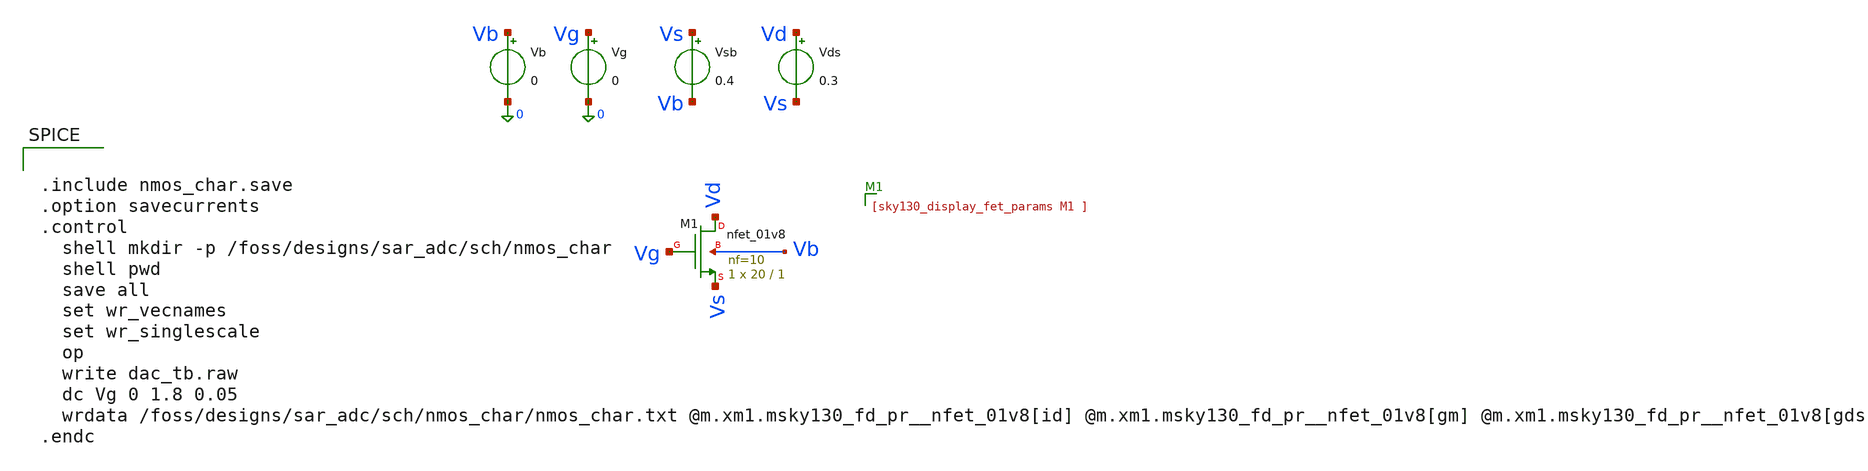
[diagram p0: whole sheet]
** sch_path: sch/archive/old/nmos_char.sch
**.subckt nmos_char
XM1 Vd Vg Vs Vb sky130_fd_pr__nfet_01v8 L=1 W=20 nf=10 ad='int((10 + 1)/2) * 20 / 10 * 0.29' as='int((10 + 2)/2) * 20 / 10 * 0.29'
+ pd='2*int((10 + 1)/2) * (20 / 10 + 0.29)' ps='2*int((10 + 2)/2) * (20 / 10 + 0.29)' nrd='0.29 / 20 '
+ nrs='0.29 / 20 ' sa=0 sb=0 sd=0 mult=1 m=1
Vsb Vs Vb 0.4
.save i(vsb)
Vds Vd Vs 0.3
.save i(vds)
Vb Vb 0 0
.save i(vb)
Vg Vg 0 0
.save i(vg)
**** begin user architecture code

** opencircuitdesign pdks install
.lib $::SKYWATER_MODELS/sky130.lib.spice tt
.include $::SKYWATER_STDCELLS/sky130_fd_sc_hd.spice



.include nmos_char.save
.option savecurrents
.control
  shell mkdir -p /foss/designs/sar_adc/sch/nmos_char
  shell pwd
  save all
  set wr_vecnames
  set wr_singlescale
  op
  write dac_tb.raw
  dc Vg 0 1.8 0.05
  wrdata /foss/designs/sar_adc/sch/nmos_char/nmos_char.txt @m.xm1.msky130_fd_pr__nfet_01v8[id]
+ @m.xm1.msky130_fd_pr__nfet_01v8[gm] @m.xm1.msky130_fd_pr__nfet_01v8[gds]
.endc


**** end user architecture code
**.ends
.end
